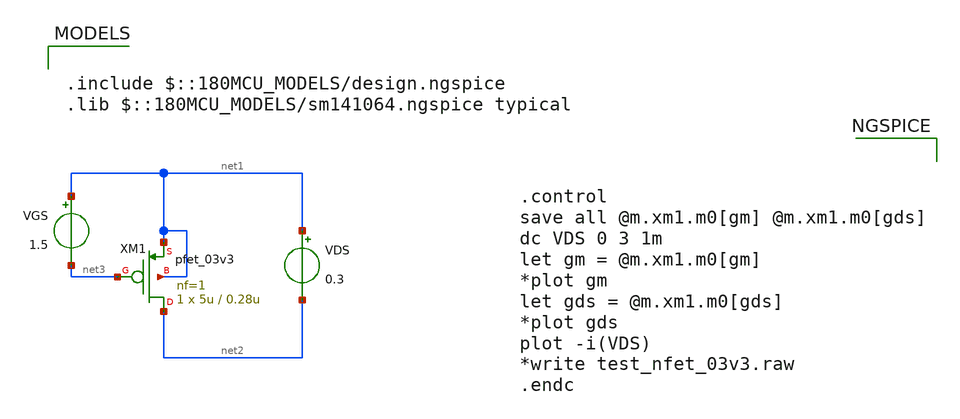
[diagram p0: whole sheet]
** sch_path: SCOP_INPUT_AND_MUX_PAKISTAN_03/Xschem/Others/pmos.sch
**.subckt pmos
VDS net1 net2 0.3
VGS net1 net3 1.5
XM1 net2 net3 net1 net1 pfet_03v3 L=0.28u W=5u nf=1 ad='int((nf+1)/2) * W/nf * 0.18u' as='int((nf+2)/2) * W/nf * 0.18u'
+ pd='2*int((nf+1)/2) * (W/nf + 0.18u)' ps='2*int((nf+2)/2) * (W/nf + 0.18u)' nrd='0.18u / W' nrs='0.18u / W'
+ sa=0 sb=0 sd=0 m=1
**** begin user architecture code



.control
save all @m.xm1.m0[gm] @m.xm1.m0[gds]
dc VDS 0 3 1m
let gm = @m.xm1.m0[gm]
*plot gm
let gds = @m.xm1.m0[gds]
*plot gds
plot -i(VDS)
*write test_nfet_03v3.raw
.endc



.include $::180MCU_MODELS/design.ngspice
.lib $::180MCU_MODELS/sm141064.ngspice typical

**** end user architecture code
**.ends
.end
